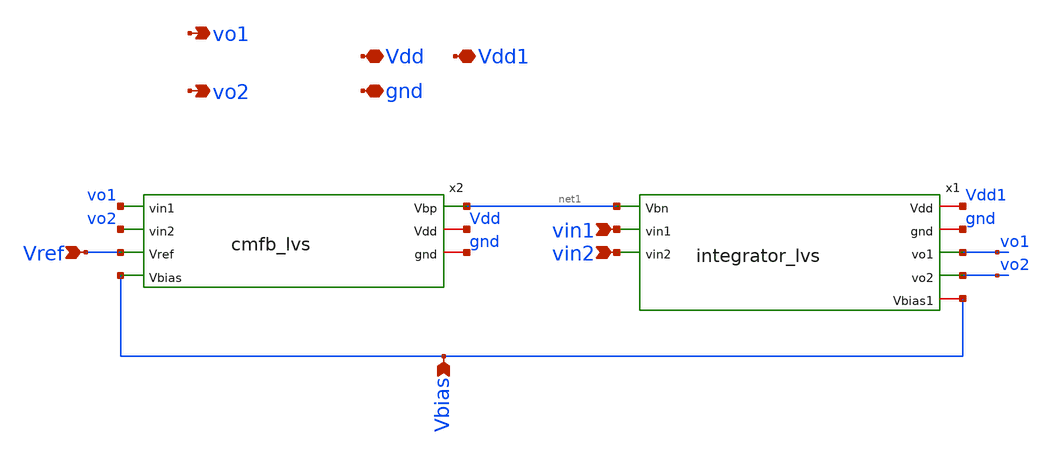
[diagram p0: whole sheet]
** sch_path: xschem/integrator_full.sch
**.subckt integrator_full vin1 vin2 gnd Vdd vo1 vo2 Vref Vbias Vdd1
*.ipin vin1
*.ipin vin2
*.iopin gnd
*.iopin Vdd
*.opin vo1
*.opin vo2
*.ipin Vref
*.ipin Vbias
*.iopin Vdd1
x1 Vdd1 gnd net1 vin1 vin2 vo1 vo2 Vbias integrator_lvs
x2 net1 Vdd gnd vo1 vo2 Vref Vbias cmfb_lvs
**.ends
.end
